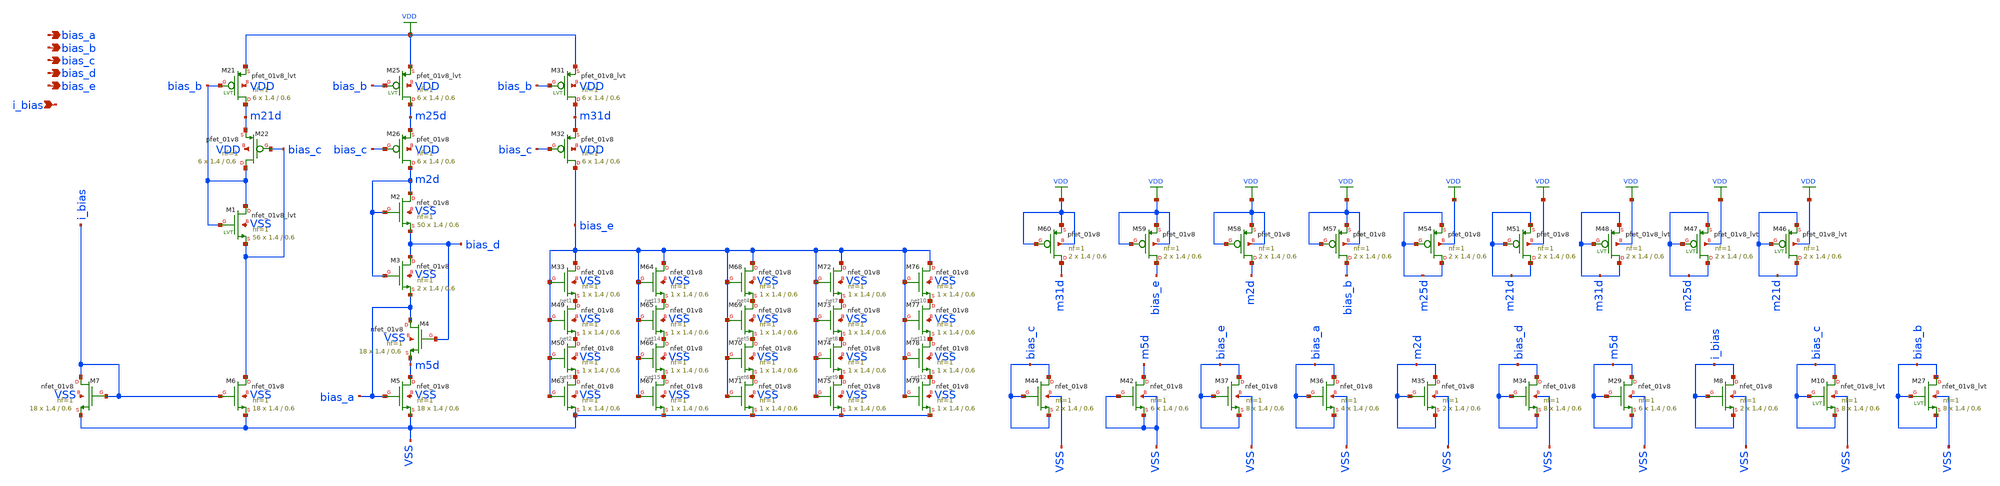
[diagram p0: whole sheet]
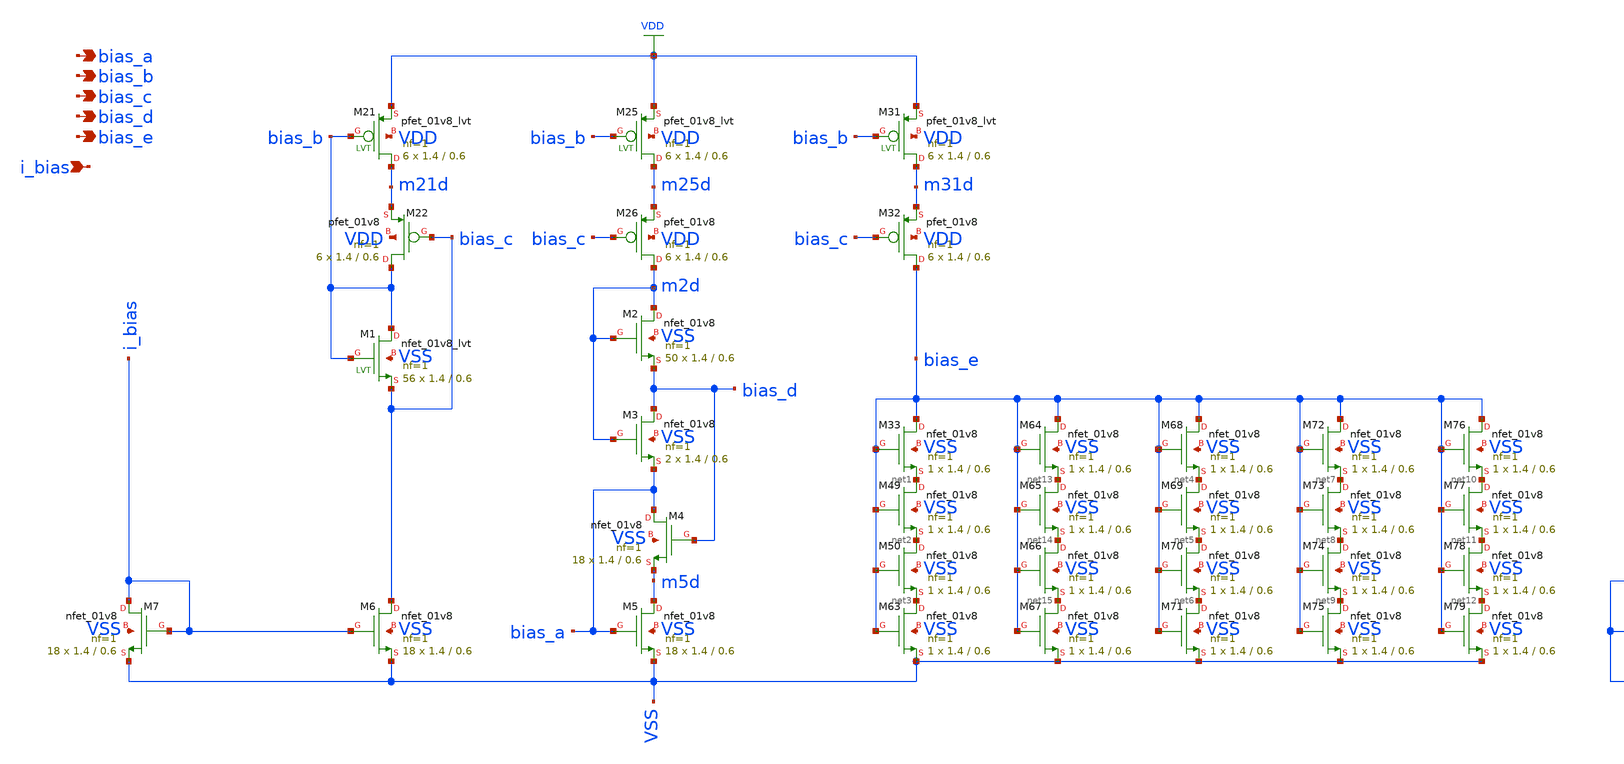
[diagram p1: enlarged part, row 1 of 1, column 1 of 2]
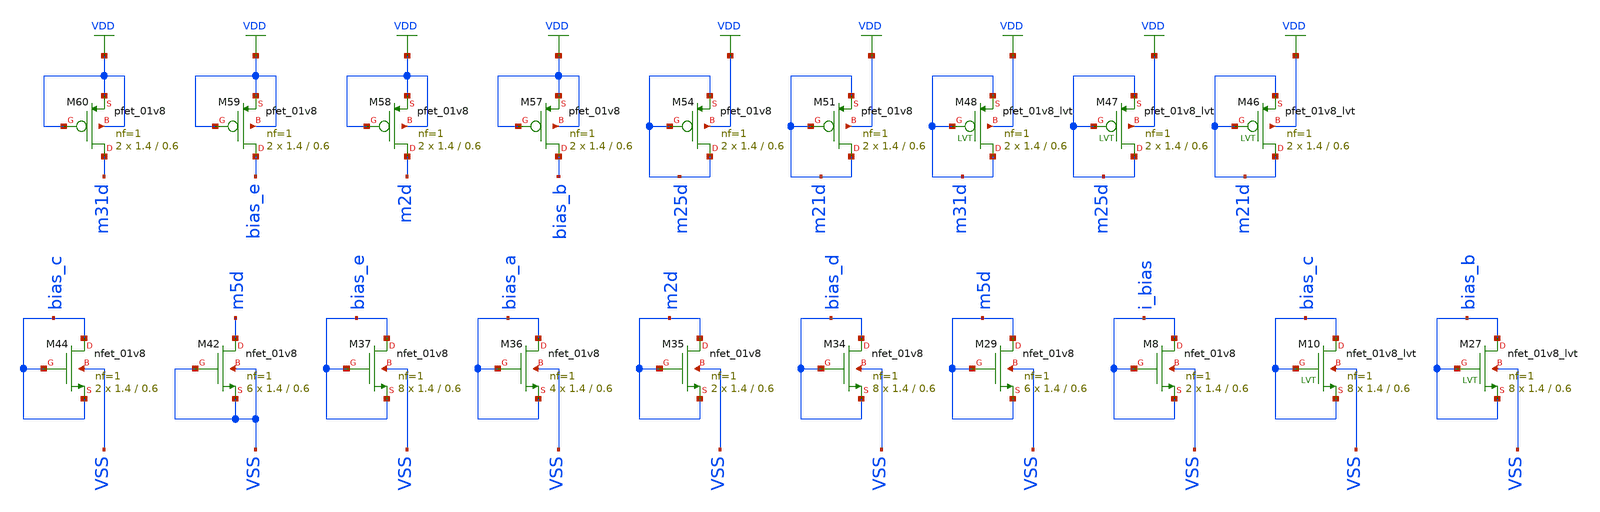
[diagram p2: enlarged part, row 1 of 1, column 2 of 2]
** sch_path: design/analog_modulator/schematic/folded_cascode_3_bias.sch
**.subckt folded_cascode_3_bias bias_a bias_b bias_c bias_d bias_e i_bias
*.opin bias_a
*.opin bias_b
*.opin bias_c
*.opin bias_d
*.opin bias_e
*.ipin i_bias
XM22 bias_b bias_c m21d VDD sky130_fd_pr__pfet_01v8 L=0.6 W=1.4 nf=1 ad='int((nf+1)/2) * W/nf * 0.29'
+ as='int((nf+2)/2) * W/nf * 0.29' pd='2*int((nf+1)/2) * (W/nf + 0.29)' ps='2*int((nf+2)/2) * (W/nf + 0.29)'
+ nrd='0.29 / W' nrs='0.29 / W' sa=0 sb=0 sd=0 mult=6 m=6
XM26 m2d bias_c m25d VDD sky130_fd_pr__pfet_01v8 L=0.6 W=1.4 nf=1 ad='int((nf+1)/2) * W/nf * 0.29' as='int((nf+2)/2) * W/nf * 0.29'
+ pd='2*int((nf+1)/2) * (W/nf + 0.29)' ps='2*int((nf+2)/2) * (W/nf + 0.29)' nrd='0.29 / W' nrs='0.29 / W'
+ sa=0 sb=0 sd=0 mult=6 m=6
XM32 bias_e bias_c m31d VDD sky130_fd_pr__pfet_01v8 L=0.6 W=1.4 nf=1 ad='int((nf+1)/2) * W/nf * 0.29'
+ as='int((nf+2)/2) * W/nf * 0.29' pd='2*int((nf+1)/2) * (W/nf + 0.29)' ps='2*int((nf+2)/2) * (W/nf + 0.29)'
+ nrd='0.29 / W' nrs='0.29 / W' sa=0 sb=0 sd=0 mult=6 m=6
XM21 m21d bias_b VDD VDD sky130_fd_pr__pfet_01v8_lvt L=0.6 W=1.4 nf=1 ad='int((nf+1)/2) * W/nf * 0.29'
+ as='int((nf+2)/2) * W/nf * 0.29' pd='2*int((nf+1)/2) * (W/nf + 0.29)' ps='2*int((nf+2)/2) * (W/nf + 0.29)'
+ nrd='0.29 / W' nrs='0.29 / W' sa=0 sb=0 sd=0 mult=6 m=6
XM25 m25d bias_b VDD VDD sky130_fd_pr__pfet_01v8_lvt L=0.6 W=1.4 nf=1 ad='int((nf+1)/2) * W/nf * 0.29'
+ as='int((nf+2)/2) * W/nf * 0.29' pd='2*int((nf+1)/2) * (W/nf + 0.29)' ps='2*int((nf+2)/2) * (W/nf + 0.29)'
+ nrd='0.29 / W' nrs='0.29 / W' sa=0 sb=0 sd=0 mult=6 m=6
XM31 m31d bias_b VDD VDD sky130_fd_pr__pfet_01v8_lvt L=0.6 W=1.4 nf=1 ad='int((nf+1)/2) * W/nf * 0.29'
+ as='int((nf+2)/2) * W/nf * 0.29' pd='2*int((nf+1)/2) * (W/nf + 0.29)' ps='2*int((nf+2)/2) * (W/nf + 0.29)'
+ nrd='0.29 / W' nrs='0.29 / W' sa=0 sb=0 sd=0 mult=6 m=6
XM1 bias_b bias_b bias_c VSS sky130_fd_pr__nfet_01v8_lvt L=0.6 W=1.4 nf=1 ad='int((nf+1)/2) * W/nf * 0.29'
+ as='int((nf+2)/2) * W/nf * 0.29' pd='2*int((nf+1)/2) * (W/nf + 0.29)' ps='2*int((nf+2)/2) * (W/nf + 0.29)'
+ nrd='0.29 / W' nrs='0.29 / W' sa=0 sb=0 sd=0 mult=56 m=56
XM2 m2d m2d bias_d VSS sky130_fd_pr__nfet_01v8 L=0.6 W=1.4 nf=1 ad='int((nf+1)/2) * W/nf * 0.29' as='int((nf+2)/2) * W/nf * 0.29'
+ pd='2*int((nf+1)/2) * (W/nf + 0.29)' ps='2*int((nf+2)/2) * (W/nf + 0.29)' nrd='0.29 / W' nrs='0.29 / W'
+ sa=0 sb=0 sd=0 mult=50 m=50
XM3 bias_d m2d bias_a VSS sky130_fd_pr__nfet_01v8 L=0.6 W=1.4 nf=1 ad='int((nf+1)/2) * W/nf * 0.29' as='int((nf+2)/2) * W/nf * 0.29'
+ pd='2*int((nf+1)/2) * (W/nf + 0.29)' ps='2*int((nf+2)/2) * (W/nf + 0.29)' nrd='0.29 / W' nrs='0.29 / W'
+ sa=0 sb=0 sd=0 mult=2 m=2
XM4 bias_a bias_d m5d VSS sky130_fd_pr__nfet_01v8 L=0.6 W=1.4 nf=1 ad='int((nf+1)/2) * W/nf * 0.29' as='int((nf+2)/2) * W/nf * 0.29'
+ pd='2*int((nf+1)/2) * (W/nf + 0.29)' ps='2*int((nf+2)/2) * (W/nf + 0.29)' nrd='0.29 / W' nrs='0.29 / W'
+ sa=0 sb=0 sd=0 mult=18 m=18
XM5 m5d bias_a VSS VSS sky130_fd_pr__nfet_01v8 L=0.6 W=1.4 nf=1 ad='int((nf+1)/2) * W/nf * 0.29' as='int((nf+2)/2) * W/nf * 0.29'
+ pd='2*int((nf+1)/2) * (W/nf + 0.29)' ps='2*int((nf+2)/2) * (W/nf + 0.29)' nrd='0.29 / W' nrs='0.29 / W'
+ sa=0 sb=0 sd=0 mult=18 m=18
XM6 bias_c i_bias VSS VSS sky130_fd_pr__nfet_01v8 L=0.6 W=1.4 nf=1 ad='int((nf+1)/2) * W/nf * 0.29' as='int((nf+2)/2) * W/nf * 0.29'
+ pd='2*int((nf+1)/2) * (W/nf + 0.29)' ps='2*int((nf+2)/2) * (W/nf + 0.29)' nrd='0.29 / W' nrs='0.29 / W'
+ sa=0 sb=0 sd=0 mult=18 m=18
XM7 i_bias i_bias VSS VSS sky130_fd_pr__nfet_01v8 L=0.6 W=1.4 nf=1 ad='int((nf+1)/2) * W/nf * 0.29' as='int((nf+2)/2) * W/nf * 0.29'
+ pd='2*int((nf+1)/2) * (W/nf + 0.29)' ps='2*int((nf+2)/2) * (W/nf + 0.29)' nrd='0.29 / W' nrs='0.29 / W'
+ sa=0 sb=0 sd=0 mult=18 m=18
XM33 bias_e bias_e net1 VSS sky130_fd_pr__nfet_01v8 L=0.6 W=1.4 nf=1 ad='int((nf+1)/2) * W/nf * 0.29'
+ as='int((nf+2)/2) * W/nf * 0.29' pd='2*int((nf+1)/2) * (W/nf + 0.29)' ps='2*int((nf+2)/2) * (W/nf + 0.29)'
+ nrd='0.29 / W' nrs='0.29 / W' sa=0 sb=0 sd=0 mult=1 m=1
XM49 net1 bias_e net2 VSS sky130_fd_pr__nfet_01v8 L=0.6 W=1.4 nf=1 ad='int((nf+1)/2) * W/nf * 0.29' as='int((nf+2)/2) * W/nf * 0.29'
+ pd='2*int((nf+1)/2) * (W/nf + 0.29)' ps='2*int((nf+2)/2) * (W/nf + 0.29)' nrd='0.29 / W' nrs='0.29 / W'
+ sa=0 sb=0 sd=0 mult=1 m=1
XM50 net2 bias_e net3 VSS sky130_fd_pr__nfet_01v8 L=0.6 W=1.4 nf=1 ad='int((nf+1)/2) * W/nf * 0.29' as='int((nf+2)/2) * W/nf * 0.29'
+ pd='2*int((nf+1)/2) * (W/nf + 0.29)' ps='2*int((nf+2)/2) * (W/nf + 0.29)' nrd='0.29 / W' nrs='0.29 / W'
+ sa=0 sb=0 sd=0 mult=1 m=1
XM63 net3 bias_e VSS VSS sky130_fd_pr__nfet_01v8 L=0.6 W=1.4 nf=1 ad='int((nf+1)/2) * W/nf * 0.29' as='int((nf+2)/2) * W/nf * 0.29'
+ pd='2*int((nf+1)/2) * (W/nf + 0.29)' ps='2*int((nf+2)/2) * (W/nf + 0.29)' nrd='0.29 / W' nrs='0.29 / W'
+ sa=0 sb=0 sd=0 mult=1 m=1
XM68 bias_e bias_e net4 VSS sky130_fd_pr__nfet_01v8 L=0.6 W=1.4 nf=1 ad='int((nf+1)/2) * W/nf * 0.29'
+ as='int((nf+2)/2) * W/nf * 0.29' pd='2*int((nf+1)/2) * (W/nf + 0.29)' ps='2*int((nf+2)/2) * (W/nf + 0.29)'
+ nrd='0.29 / W' nrs='0.29 / W' sa=0 sb=0 sd=0 mult=1 m=1
XM69 net4 bias_e net5 VSS sky130_fd_pr__nfet_01v8 L=0.6 W=1.4 nf=1 ad='int((nf+1)/2) * W/nf * 0.29' as='int((nf+2)/2) * W/nf * 0.29'
+ pd='2*int((nf+1)/2) * (W/nf + 0.29)' ps='2*int((nf+2)/2) * (W/nf + 0.29)' nrd='0.29 / W' nrs='0.29 / W'
+ sa=0 sb=0 sd=0 mult=1 m=1
XM70 net5 bias_e net6 VSS sky130_fd_pr__nfet_01v8 L=0.6 W=1.4 nf=1 ad='int((nf+1)/2) * W/nf * 0.29' as='int((nf+2)/2) * W/nf * 0.29'
+ pd='2*int((nf+1)/2) * (W/nf + 0.29)' ps='2*int((nf+2)/2) * (W/nf + 0.29)' nrd='0.29 / W' nrs='0.29 / W'
+ sa=0 sb=0 sd=0 mult=1 m=1
XM71 net6 bias_e VSS VSS sky130_fd_pr__nfet_01v8 L=0.6 W=1.4 nf=1 ad='int((nf+1)/2) * W/nf * 0.29' as='int((nf+2)/2) * W/nf * 0.29'
+ pd='2*int((nf+1)/2) * (W/nf + 0.29)' ps='2*int((nf+2)/2) * (W/nf + 0.29)' nrd='0.29 / W' nrs='0.29 / W'
+ sa=0 sb=0 sd=0 mult=1 m=1
XM72 bias_e bias_e net7 VSS sky130_fd_pr__nfet_01v8 L=0.6 W=1.4 nf=1 ad='int((nf+1)/2) * W/nf * 0.29'
+ as='int((nf+2)/2) * W/nf * 0.29' pd='2*int((nf+1)/2) * (W/nf + 0.29)' ps='2*int((nf+2)/2) * (W/nf + 0.29)'
+ nrd='0.29 / W' nrs='0.29 / W' sa=0 sb=0 sd=0 mult=1 m=1
XM73 net7 bias_e net8 VSS sky130_fd_pr__nfet_01v8 L=0.6 W=1.4 nf=1 ad='int((nf+1)/2) * W/nf * 0.29' as='int((nf+2)/2) * W/nf * 0.29'
+ pd='2*int((nf+1)/2) * (W/nf + 0.29)' ps='2*int((nf+2)/2) * (W/nf + 0.29)' nrd='0.29 / W' nrs='0.29 / W'
+ sa=0 sb=0 sd=0 mult=1 m=1
XM74 net8 bias_e net9 VSS sky130_fd_pr__nfet_01v8 L=0.6 W=1.4 nf=1 ad='int((nf+1)/2) * W/nf * 0.29' as='int((nf+2)/2) * W/nf * 0.29'
+ pd='2*int((nf+1)/2) * (W/nf + 0.29)' ps='2*int((nf+2)/2) * (W/nf + 0.29)' nrd='0.29 / W' nrs='0.29 / W'
+ sa=0 sb=0 sd=0 mult=1 m=1
XM75 net9 bias_e VSS VSS sky130_fd_pr__nfet_01v8 L=0.6 W=1.4 nf=1 ad='int((nf+1)/2) * W/nf * 0.29' as='int((nf+2)/2) * W/nf * 0.29'
+ pd='2*int((nf+1)/2) * (W/nf + 0.29)' ps='2*int((nf+2)/2) * (W/nf + 0.29)' nrd='0.29 / W' nrs='0.29 / W'
+ sa=0 sb=0 sd=0 mult=1 m=1
XM76 bias_e bias_e net10 VSS sky130_fd_pr__nfet_01v8 L=0.6 W=1.4 nf=1 ad='int((nf+1)/2) * W/nf * 0.29'
+ as='int((nf+2)/2) * W/nf * 0.29' pd='2*int((nf+1)/2) * (W/nf + 0.29)' ps='2*int((nf+2)/2) * (W/nf + 0.29)'
+ nrd='0.29 / W' nrs='0.29 / W' sa=0 sb=0 sd=0 mult=1 m=1
XM77 net10 bias_e net11 VSS sky130_fd_pr__nfet_01v8 L=0.6 W=1.4 nf=1 ad='int((nf+1)/2) * W/nf * 0.29'
+ as='int((nf+2)/2) * W/nf * 0.29' pd='2*int((nf+1)/2) * (W/nf + 0.29)' ps='2*int((nf+2)/2) * (W/nf + 0.29)'
+ nrd='0.29 / W' nrs='0.29 / W' sa=0 sb=0 sd=0 mult=1 m=1
XM78 net11 bias_e net12 VSS sky130_fd_pr__nfet_01v8 L=0.6 W=1.4 nf=1 ad='int((nf+1)/2) * W/nf * 0.29'
+ as='int((nf+2)/2) * W/nf * 0.29' pd='2*int((nf+1)/2) * (W/nf + 0.29)' ps='2*int((nf+2)/2) * (W/nf + 0.29)'
+ nrd='0.29 / W' nrs='0.29 / W' sa=0 sb=0 sd=0 mult=1 m=1
XM79 net12 bias_e VSS VSS sky130_fd_pr__nfet_01v8 L=0.6 W=1.4 nf=1 ad='int((nf+1)/2) * W/nf * 0.29' as='int((nf+2)/2) * W/nf * 0.29'
+ pd='2*int((nf+1)/2) * (W/nf + 0.29)' ps='2*int((nf+2)/2) * (W/nf + 0.29)' nrd='0.29 / W' nrs='0.29 / W'
+ sa=0 sb=0 sd=0 mult=1 m=1
XM64 bias_e bias_e net13 VSS sky130_fd_pr__nfet_01v8 L=0.6 W=1.4 nf=1 ad='int((nf+1)/2) * W/nf * 0.29'
+ as='int((nf+2)/2) * W/nf * 0.29' pd='2*int((nf+1)/2) * (W/nf + 0.29)' ps='2*int((nf+2)/2) * (W/nf + 0.29)'
+ nrd='0.29 / W' nrs='0.29 / W' sa=0 sb=0 sd=0 mult=1 m=1
XM65 net13 bias_e net14 VSS sky130_fd_pr__nfet_01v8 L=0.6 W=1.4 nf=1 ad='int((nf+1)/2) * W/nf * 0.29'
+ as='int((nf+2)/2) * W/nf * 0.29' pd='2*int((nf+1)/2) * (W/nf + 0.29)' ps='2*int((nf+2)/2) * (W/nf + 0.29)'
+ nrd='0.29 / W' nrs='0.29 / W' sa=0 sb=0 sd=0 mult=1 m=1
XM66 net14 bias_e net15 VSS sky130_fd_pr__nfet_01v8 L=0.6 W=1.4 nf=1 ad='int((nf+1)/2) * W/nf * 0.29'
+ as='int((nf+2)/2) * W/nf * 0.29' pd='2*int((nf+1)/2) * (W/nf + 0.29)' ps='2*int((nf+2)/2) * (W/nf + 0.29)'
+ nrd='0.29 / W' nrs='0.29 / W' sa=0 sb=0 sd=0 mult=1 m=1
XM67 net15 bias_e VSS VSS sky130_fd_pr__nfet_01v8 L=0.6 W=1.4 nf=1 ad='int((nf+1)/2) * W/nf * 0.29' as='int((nf+2)/2) * W/nf * 0.29'
+ pd='2*int((nf+1)/2) * (W/nf + 0.29)' ps='2*int((nf+2)/2) * (W/nf + 0.29)' nrd='0.29 / W' nrs='0.29 / W'
+ sa=0 sb=0 sd=0 mult=1 m=1
XM57 bias_b VDD VDD VDD sky130_fd_pr__pfet_01v8 L=0.6 W=1.4 nf=1 ad='int((nf+1)/2) * W/nf * 0.29' as='int((nf+2)/2) * W/nf * 0.29'
+ pd='2*int((nf+1)/2) * (W/nf + 0.29)' ps='2*int((nf+2)/2) * (W/nf + 0.29)' nrd='0.29 / W' nrs='0.29 / W'
+ sa=0 sb=0 sd=0 mult=2 m=2
XM58 m2d VDD VDD VDD sky130_fd_pr__pfet_01v8 L=0.6 W=1.4 nf=1 ad='int((nf+1)/2) * W/nf * 0.29' as='int((nf+2)/2) * W/nf * 0.29'
+ pd='2*int((nf+1)/2) * (W/nf + 0.29)' ps='2*int((nf+2)/2) * (W/nf + 0.29)' nrd='0.29 / W' nrs='0.29 / W'
+ sa=0 sb=0 sd=0 mult=2 m=2
XM59 bias_e VDD VDD VDD sky130_fd_pr__pfet_01v8 L=0.6 W=1.4 nf=1 ad='int((nf+1)/2) * W/nf * 0.29' as='int((nf+2)/2) * W/nf * 0.29'
+ pd='2*int((nf+1)/2) * (W/nf + 0.29)' ps='2*int((nf+2)/2) * (W/nf + 0.29)' nrd='0.29 / W' nrs='0.29 / W'
+ sa=0 sb=0 sd=0 mult=2 m=2
XM60 m31d VDD VDD VDD sky130_fd_pr__pfet_01v8 L=0.6 W=1.4 nf=1 ad='int((nf+1)/2) * W/nf * 0.29' as='int((nf+2)/2) * W/nf * 0.29'
+ pd='2*int((nf+1)/2) * (W/nf + 0.29)' ps='2*int((nf+2)/2) * (W/nf + 0.29)' nrd='0.29 / W' nrs='0.29 / W'
+ sa=0 sb=0 sd=0 mult=2 m=2
XM42 m5d VSS VSS VSS sky130_fd_pr__nfet_01v8 L=0.6 W=1.4 nf=1 ad='int((nf+1)/2) * W/nf * 0.29' as='int((nf+2)/2) * W/nf * 0.29'
+ pd='2*int((nf+1)/2) * (W/nf + 0.29)' ps='2*int((nf+2)/2) * (W/nf + 0.29)' nrd='0.29 / W' nrs='0.29 / W'
+ sa=0 sb=0 sd=0 mult=6 m=6
XM44 bias_c bias_c bias_c VSS sky130_fd_pr__nfet_01v8 L=0.6 W=1.4 nf=1 ad='int((nf+1)/2) * W/nf * 0.29'
+ as='int((nf+2)/2) * W/nf * 0.29' pd='2*int((nf+1)/2) * (W/nf + 0.29)' ps='2*int((nf+2)/2) * (W/nf + 0.29)'
+ nrd='0.29 / W' nrs='0.29 / W' sa=0 sb=0 sd=0 mult=2 m=2
XM34 bias_d bias_d bias_d VSS sky130_fd_pr__nfet_01v8 L=0.6 W=1.4 nf=1 ad='int((nf+1)/2) * W/nf * 0.29'
+ as='int((nf+2)/2) * W/nf * 0.29' pd='2*int((nf+1)/2) * (W/nf + 0.29)' ps='2*int((nf+2)/2) * (W/nf + 0.29)'
+ nrd='0.29 / W' nrs='0.29 / W' sa=0 sb=0 sd=0 mult=8 m=8
XM35 m2d m2d m2d VSS sky130_fd_pr__nfet_01v8 L=0.6 W=1.4 nf=1 ad='int((nf+1)/2) * W/nf * 0.29' as='int((nf+2)/2) * W/nf * 0.29'
+ pd='2*int((nf+1)/2) * (W/nf + 0.29)' ps='2*int((nf+2)/2) * (W/nf + 0.29)' nrd='0.29 / W' nrs='0.29 / W'
+ sa=0 sb=0 sd=0 mult=2 m=2
XM36 bias_a bias_a bias_a VSS sky130_fd_pr__nfet_01v8 L=0.6 W=1.4 nf=1 ad='int((nf+1)/2) * W/nf * 0.29'
+ as='int((nf+2)/2) * W/nf * 0.29' pd='2*int((nf+1)/2) * (W/nf + 0.29)' ps='2*int((nf+2)/2) * (W/nf + 0.29)'
+ nrd='0.29 / W' nrs='0.29 / W' sa=0 sb=0 sd=0 mult=4 m=4
XM37 bias_e bias_e bias_e VSS sky130_fd_pr__nfet_01v8 L=0.6 W=1.4 nf=1 ad='int((nf+1)/2) * W/nf * 0.29'
+ as='int((nf+2)/2) * W/nf * 0.29' pd='2*int((nf+1)/2) * (W/nf + 0.29)' ps='2*int((nf+2)/2) * (W/nf + 0.29)'
+ nrd='0.29 / W' nrs='0.29 / W' sa=0 sb=0 sd=0 mult=8 m=8
XM54 m25d m25d m25d VDD sky130_fd_pr__pfet_01v8 L=0.6 W=1.4 nf=1 ad='int((nf+1)/2) * W/nf * 0.29' as='int((nf+2)/2) * W/nf * 0.29'
+ pd='2*int((nf+1)/2) * (W/nf + 0.29)' ps='2*int((nf+2)/2) * (W/nf + 0.29)' nrd='0.29 / W' nrs='0.29 / W'
+ sa=0 sb=0 sd=0 mult=2 m=2
XM29 m5d m5d m5d VSS sky130_fd_pr__nfet_01v8 L=0.6 W=1.4 nf=1 ad='int((nf+1)/2) * W/nf * 0.29' as='int((nf+2)/2) * W/nf * 0.29'
+ pd='2*int((nf+1)/2) * (W/nf + 0.29)' ps='2*int((nf+2)/2) * (W/nf + 0.29)' nrd='0.29 / W' nrs='0.29 / W'
+ sa=0 sb=0 sd=0 mult=6 m=6
XM8 i_bias i_bias i_bias VSS sky130_fd_pr__nfet_01v8 L=0.6 W=1.4 nf=1 ad='int((nf+1)/2) * W/nf * 0.29'
+ as='int((nf+2)/2) * W/nf * 0.29' pd='2*int((nf+1)/2) * (W/nf + 0.29)' ps='2*int((nf+2)/2) * (W/nf + 0.29)'
+ nrd='0.29 / W' nrs='0.29 / W' sa=0 sb=0 sd=0 mult=2 m=2
XM10 bias_c bias_c bias_c VSS sky130_fd_pr__nfet_01v8_lvt L=0.6 W=1.4 nf=1 ad='int((nf+1)/2) * W/nf * 0.29'
+ as='int((nf+2)/2) * W/nf * 0.29' pd='2*int((nf+1)/2) * (W/nf + 0.29)' ps='2*int((nf+2)/2) * (W/nf + 0.29)'
+ nrd='0.29 / W' nrs='0.29 / W' sa=0 sb=0 sd=0 mult=8 m=8
XM27 bias_b bias_b bias_b VSS sky130_fd_pr__nfet_01v8_lvt L=0.6 W=1.4 nf=1 ad='int((nf+1)/2) * W/nf * 0.29'
+ as='int((nf+2)/2) * W/nf * 0.29' pd='2*int((nf+1)/2) * (W/nf + 0.29)' ps='2*int((nf+2)/2) * (W/nf + 0.29)'
+ nrd='0.29 / W' nrs='0.29 / W' sa=0 sb=0 sd=0 mult=8 m=8
XM46 m21d m21d m21d VDD sky130_fd_pr__pfet_01v8_lvt L=0.6 W=1.4 nf=1 ad='int((nf+1)/2) * W/nf * 0.29'
+ as='int((nf+2)/2) * W/nf * 0.29' pd='2*int((nf+1)/2) * (W/nf + 0.29)' ps='2*int((nf+2)/2) * (W/nf + 0.29)'
+ nrd='0.29 / W' nrs='0.29 / W' sa=0 sb=0 sd=0 mult=2 m=2
XM47 m25d m25d m25d VDD sky130_fd_pr__pfet_01v8_lvt L=0.6 W=1.4 nf=1 ad='int((nf+1)/2) * W/nf * 0.29'
+ as='int((nf+2)/2) * W/nf * 0.29' pd='2*int((nf+1)/2) * (W/nf + 0.29)' ps='2*int((nf+2)/2) * (W/nf + 0.29)'
+ nrd='0.29 / W' nrs='0.29 / W' sa=0 sb=0 sd=0 mult=2 m=2
XM48 m31d m31d m31d VDD sky130_fd_pr__pfet_01v8_lvt L=0.6 W=1.4 nf=1 ad='int((nf+1)/2) * W/nf * 0.29'
+ as='int((nf+2)/2) * W/nf * 0.29' pd='2*int((nf+1)/2) * (W/nf + 0.29)' ps='2*int((nf+2)/2) * (W/nf + 0.29)'
+ nrd='0.29 / W' nrs='0.29 / W' sa=0 sb=0 sd=0 mult=2 m=2
XM51 m21d m21d m21d VDD sky130_fd_pr__pfet_01v8 L=0.6 W=1.4 nf=1 ad='int((nf+1)/2) * W/nf * 0.29' as='int((nf+2)/2) * W/nf * 0.29'
+ pd='2*int((nf+1)/2) * (W/nf + 0.29)' ps='2*int((nf+2)/2) * (W/nf + 0.29)' nrd='0.29 / W' nrs='0.29 / W'
+ sa=0 sb=0 sd=0 mult=2 m=2
**.ends
.GLOBAL VDD
.end
